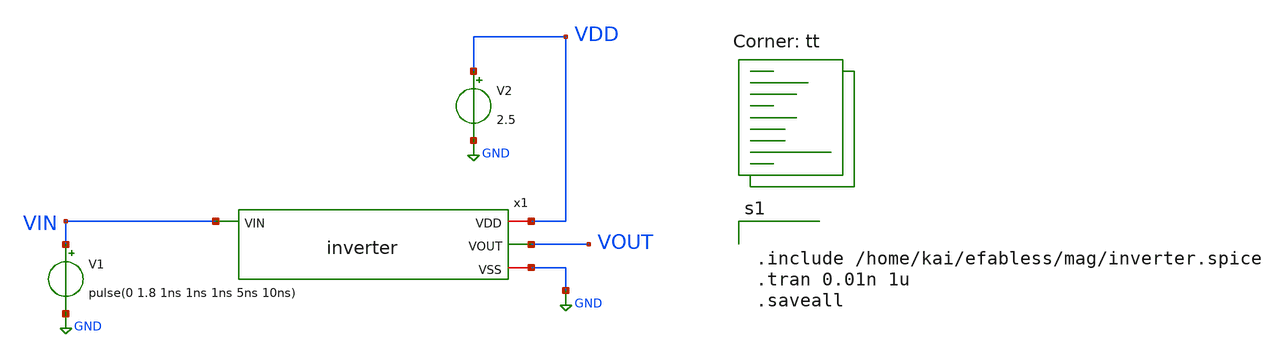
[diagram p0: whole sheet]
** sch_path: xschem/inverter_tb.sch
**.subckt inverter_tb
x1 VDD VIN VOUT GND inverter
V1 VIN GND pulse(0 1.8 1ns 1ns 1ns 5ns 10ns)
V2 VDD GND 2.5
**** begin user architecture code


.include /home/kai/efabless/mag/inverter.spice
.tran 0.01n 1u
.saveall

.lib $::SKYWATER_MODELS/sky130.lib.spice tt
**** end user architecture code
**.ends

* expanding   symbol:  inverter.sym # of pins=4
** sym_path: xschem/inverter.sym
** sch_path: xschem/inverter.sch
.subckt inverter VDD VIN VOUT VSS
*.ipin VIN
*.opin VOUT
*.iopin VDD
*.iopin VSS
XM1 VOUT VIN VSS VSS sky130_fd_pr__nfet_g5v0d10v5 L=0.5 W=1 nf=1 ad='int((nf+1)/2) * W/nf * 0.29' as='int((nf+2)/2) * W/nf * 0.29'
+ pd='2*int((nf+1)/2) * (W/nf + 0.29)' ps='2*int((nf+2)/2) * (W/nf + 0.29)' nrd='0.29 / W' nrs='0.29 / W'
+ sa=0 sb=0 sd=0 mult=1 m=1
XM2 VOUT VIN VDD VDD sky130_fd_pr__pfet_g5v0d10v5 L=0.5 W=1 nf=1 ad='int((nf+1)/2) * W/nf * 0.29' as='int((nf+2)/2) * W/nf * 0.29'
+ pd='2*int((nf+1)/2) * (W/nf + 0.29)' ps='2*int((nf+2)/2) * (W/nf + 0.29)' nrd='0.29 / W' nrs='0.29 / W'
+ sa=0 sb=0 sd=0 mult=1 m=1
.ends

.GLOBAL GND
.end
